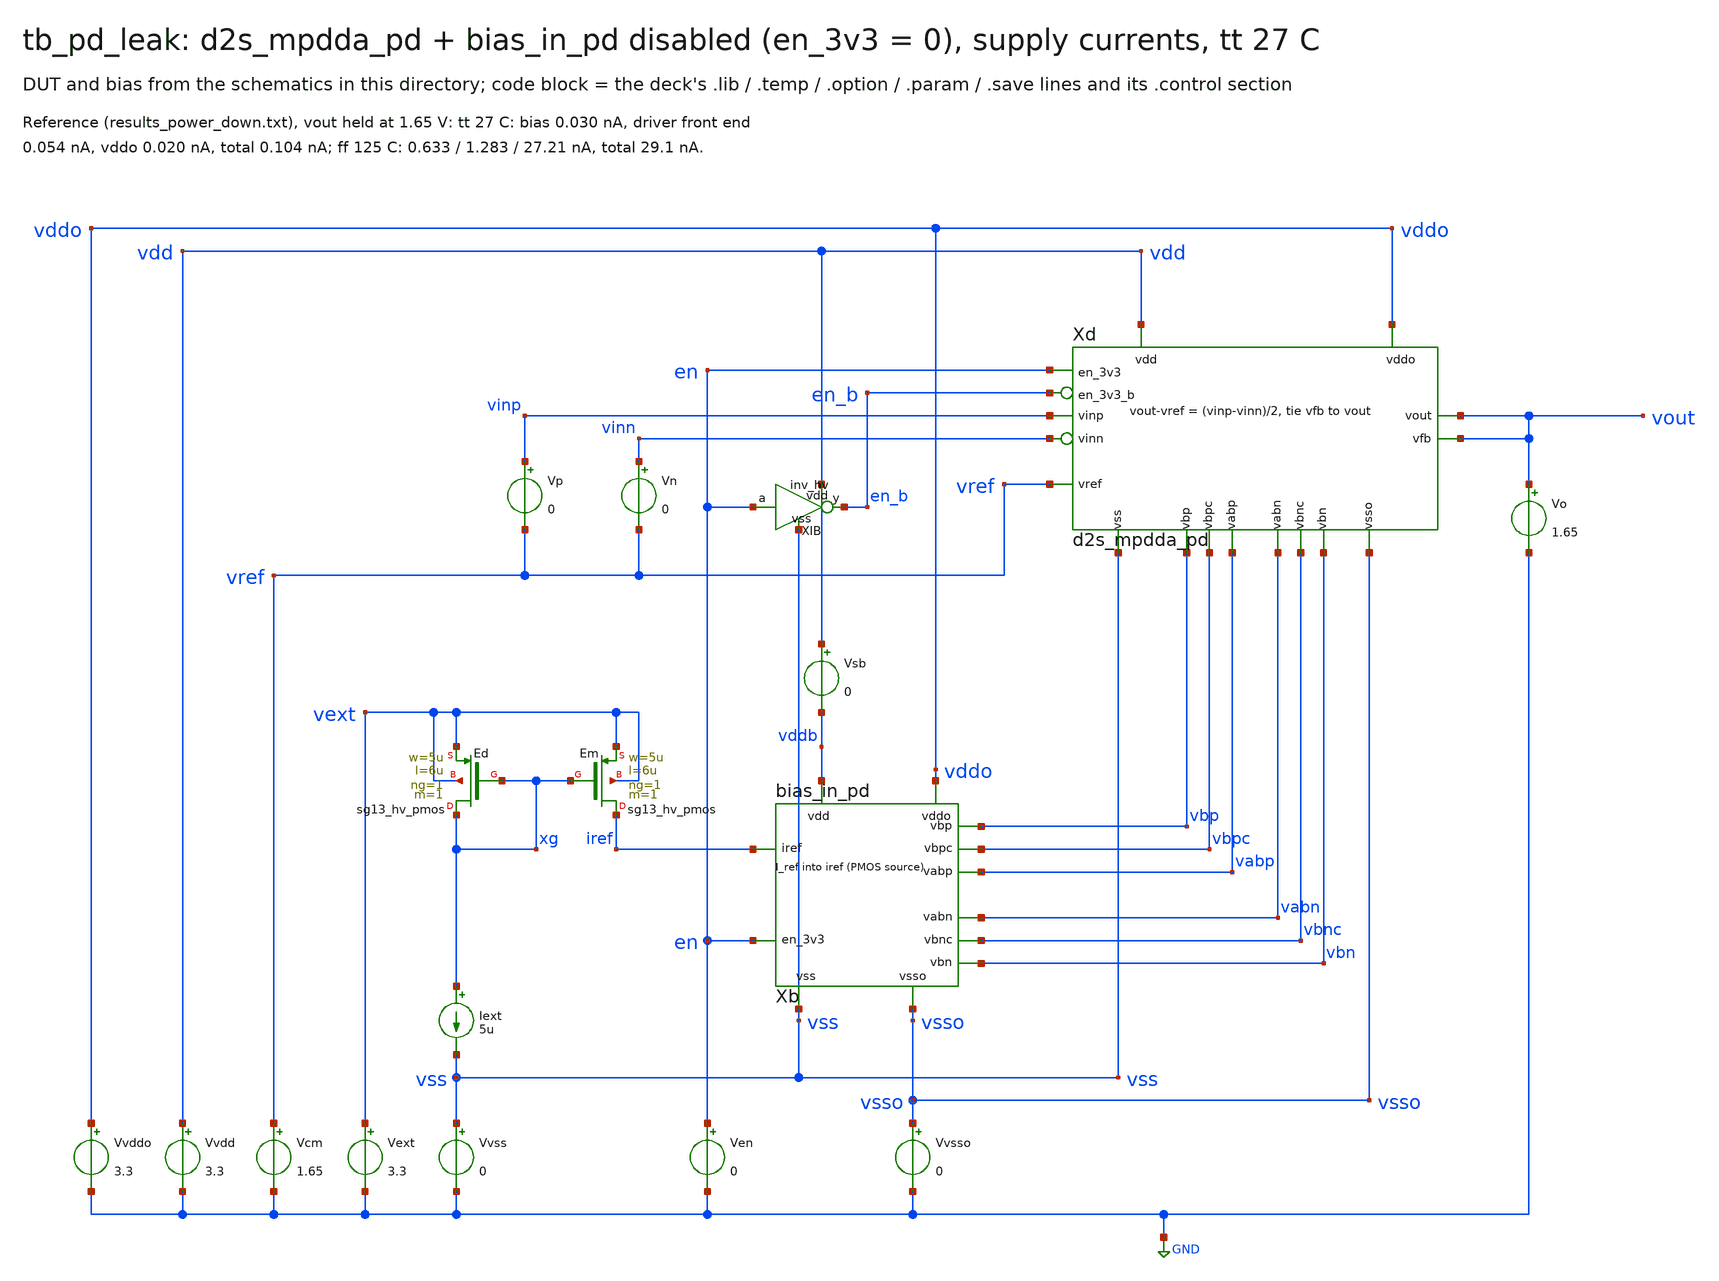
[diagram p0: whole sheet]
** sch_path: sudelbuecher/design_considerations/consolidation/ab_regroup_2026-10-28/before/macros/sg13cmos5l_IOPadDiff2Single/testbenches/xschem/tb_pd_leak.sch
**.subckt tb_pd_leak
Vvdd vdd GND 3.3
Vvss vss GND 0
Vvddo vddo GND 3.3
Vvsso vsso GND 0
Ven en GND 0
Vext vext GND 3.3
Vcm vref GND 1.65
Xb vddb vss vddo vsso iref vbp vbn vbpc vbnc vabp vabn en bias_in_pd
Xd vdd vss vddo vsso vinp vinn vref vout vout vbp vbn vbpc vbnc vabp vabn en en_b d2s_mpdda_pd
Vp vinp vref 0
Vn vinn vref 0
XEd xg xg vext vext sg13_hv_pmos w=5u l=6u ng=1 m=1 mm_ok=1
XEm iref xg vext vext sg13_hv_pmos w=5u l=6u ng=1 m=1 mm_ok=1
Iext xg vss 5u
Vsb vdd vddb 0
Vo vout GND 1.65
XIB vdd vss en en_b inv_hv
**** begin user architecture code

.lib cornerMOShv.lib mos_tt
.lib cornerRES.lib res_typ
.lib cornerCAP.lib cap_typ
.temp 27
.control
op
let ibias = i(vsb)
let idrv = -i(vvdd) - i(vsb)
let iddo = -i(vvddo)
let itot = -i(vvdd) - i(vvddo)
let vsg_op = v(vddo) - v(xd.a)
let vgs_on = v(xd.b) - v(vsso)
print ibias idrv iddo itot vsg_op vgs_on
print v(vbp) v(vbpc) v(vabp) v(vabn) v(vbn) v(vbnc)
.endc

**** end user architecture code
**.ends
.GLOBAL GND
.end
